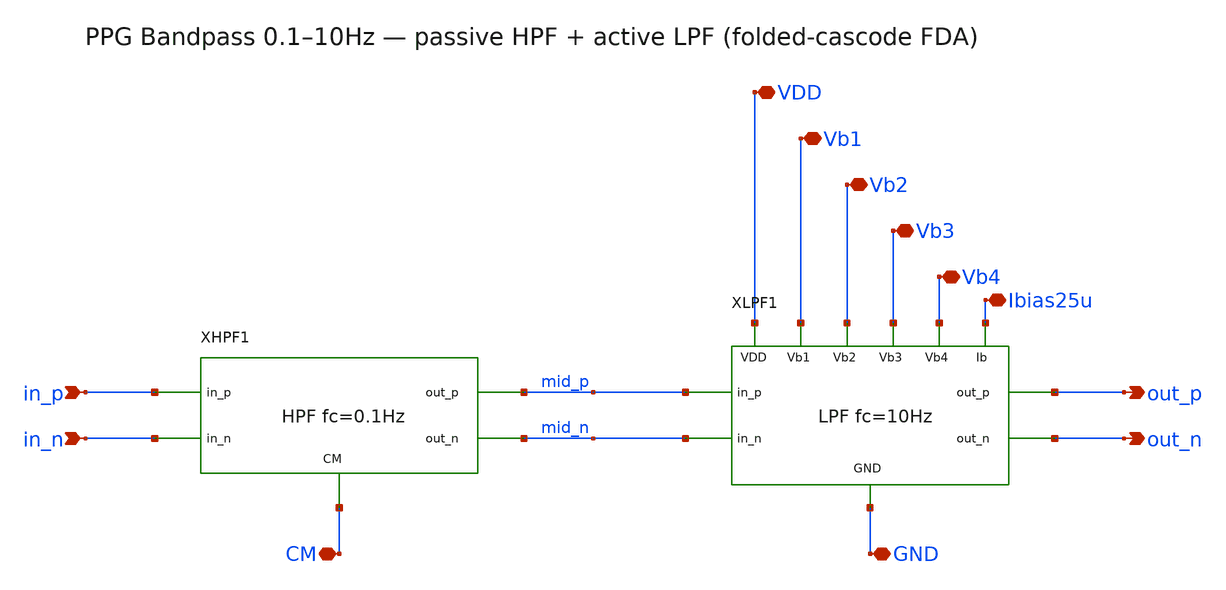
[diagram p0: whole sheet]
** sch_path: ps-filters/bandpass.sch
**.subckt bandpass in_p in_n out_p out_n CM GND VDD Vb1 Vb2 Vb3 Vb4 Ibias25u
*.ipin in_p
*.ipin in_n
*.opin out_p
*.opin out_n
*.iopin CM
*.iopin GND
*.iopin VDD
*.iopin Vb1
*.iopin Vb2
*.iopin Vb3
*.iopin Vb4
*.iopin Ibias25u
XHPF1 in_p in_n mid_p mid_n CM hpf
XLPF1 mid_p mid_n out_p out_n VDD Vb1 Vb2 Vb3 Vb4 Ibias25u GND lpf
**.ends

* expanding   symbol:  hpf.sym # of pins=5
** sym_path: ps-filters/hpf.sym
** sch_path: ps-filters/hpf.sch
.subckt hpf in_p in_n out_p out_n CM
*.ipin in_p
*.ipin in_n
*.opin out_p
*.opin out_n
*.iopin CM
Chp out_p in_p 1.59u m=1
Chn out_n in_n 1.59u m=1
Rhp out_p CM 1G m=1
Rhn out_n CM 1G m=1
.ends


* expanding   symbol:  lpf.sym # of pins=11
** sym_path: ps-filters/lpf.sym
** sch_path: ps-filters/lpf.sch
.subckt lpf in_p in_n out_p out_n VDD Vb1 Vb2 Vb3 Vb4 Ibias25u GND
*.ipin in_p
*.ipin in_n
*.opin out_p
*.opin out_n
*.iopin VDD
*.iopin GND
*.iopin Vb1
*.iopin Vb2
*.iopin Vb3
*.iopin Vb4
*.iopin Ibias25u
R1p Xp in_p 1Meg m=1
R1n Xn in_n 1Meg m=1
Rfp out_n Xp 1Meg m=1
Rfn out_p Xn 1Meg m=1
Cfp out_n Xp 15.9n m=1
Cfn out_p Xn 15.9n m=1
XFDA1 VDD Vb2 out_p out_n Vb1 Ibias25u Xn GND Xp Vb3 Vb4 foldedcasc_cmfb_forsym
.ends


* expanding   symbol:  foldedcasc_cmfb_forsym.sym # of pins=11
** sym_path: ps-filters/foldedcasc_cmfb_forsym.sym
** sch_path: ps-filters/foldedcasc_cmfb_forsym.sch
.subckt foldedcasc_cmfb_forsym VDD Vb2 Voutp Voutn Vb1 Ibias25u Vinn GND Vinp Vb3 Vb4
*.ipin VDD
*.opin Voutp
*.ipin Vinn
*.ipin Ibias25u
*.ipin GND
*.ipin Vinp
*.opin Voutn
*.ipin Vb4
*.ipin Vb1
*.ipin Vb2
*.ipin Vb3
XM5 net1 Vb3 GND GND nfet_03v3 L=0.28u W=13u nf=1 ad='int((nf+1)/2) * W/nf * 0.18u' as='int((nf+2)/2) * W/nf * 0.18u'
+ pd='2*int((nf+1)/2) * (W/nf + 0.18u)' ps='2*int((nf+2)/2) * (W/nf + 0.18u)' nrd='0.18u / W' nrs='0.18u / W'
+ sa=0 sb=0 sd=0 m=1
XM6 Voutn Vb2 net2 GND nfet_03v3 L=0.28u W=6.3u nf=1 ad='int((nf+1)/2) * W/nf * 0.18u' as='int((nf+2)/2) * W/nf * 0.18u'
+ pd='2*int((nf+1)/2) * (W/nf + 0.18u)' ps='2*int((nf+2)/2) * (W/nf + 0.18u)' nrd='0.18u / W' nrs='0.18u / W'
+ sa=0 sb=0 sd=0 m=1
XM7 Voutp Vb2 net1 GND nfet_03v3 L=0.28u W=6.3u nf=1 ad='int((nf+1)/2) * W/nf * 0.18u' as='int((nf+2)/2) * W/nf * 0.18u'
+ pd='2*int((nf+1)/2) * (W/nf + 0.18u)' ps='2*int((nf+2)/2) * (W/nf + 0.18u)' nrd='0.18u / W' nrs='0.18u / W'
+ sa=0 sb=0 sd=0 m=1
XM8 Voutn Vb1 net3 VDD pfet_03v3 L=0.28u W=19u nf=1 ad='int((nf+1)/2) * W/nf * 0.18u' as='int((nf+2)/2) * W/nf * 0.18u'
+ pd='2*int((nf+1)/2) * (W/nf + 0.18u)' ps='2*int((nf+2)/2) * (W/nf + 0.18u)' nrd='0.18u / W' nrs='0.18u / W'
+ sa=0 sb=0 sd=0 m=1
XM9 Voutp Vb1 net4 VDD pfet_03v3 L=0.28u W=19u nf=1 ad='int((nf+1)/2) * W/nf * 0.18u' as='int((nf+2)/2) * W/nf * 0.18u'
+ pd='2*int((nf+1)/2) * (W/nf + 0.18u)' ps='2*int((nf+2)/2) * (W/nf + 0.18u)' nrd='0.18u / W' nrs='0.18u / W'
+ sa=0 sb=0 sd=0 m=1
XM10 net3 Vb4 VDD VDD pfet_03v3 L=0.28u W=16.2u nf=1 ad='int((nf+1)/2) * W/nf * 0.18u' as='int((nf+2)/2) * W/nf * 0.18u'
+ pd='2*int((nf+1)/2) * (W/nf + 0.18u)' ps='2*int((nf+2)/2) * (W/nf + 0.18u)' nrd='0.18u / W' nrs='0.18u / W'
+ sa=0 sb=0 sd=0 m=1
XM11 net4 Vb4 VDD VDD pfet_03v3 L=0.28u W=16.2u nf=1 ad='int((nf+1)/2) * W/nf * 0.18u' as='int((nf+2)/2) * W/nf * 0.18u'
+ pd='2*int((nf+1)/2) * (W/nf + 0.18u)' ps='2*int((nf+2)/2) * (W/nf + 0.18u)' nrd='0.18u / W' nrs='0.18u / W'
+ sa=0 sb=0 sd=0 m=1
XM1 net1 Vinn net5 VDD pfet_03v3 L=0.28u W=3.45u nf=1 ad='int((nf+1)/2) * W/nf * 0.18u' as='int((nf+2)/2) * W/nf * 0.18u'
+ pd='2*int((nf+1)/2) * (W/nf + 0.18u)' ps='2*int((nf+2)/2) * (W/nf + 0.18u)' nrd='0.18u / W' nrs='0.18u / W'
+ sa=0 sb=0 sd=0 m=1
XM2 net2 Vinp net5 VDD pfet_03v3 L=0.28u W=3.45u nf=1 ad='int((nf+1)/2) * W/nf * 0.18u' as='int((nf+2)/2) * W/nf * 0.18u'
+ pd='2*int((nf+1)/2) * (W/nf + 0.18u)' ps='2*int((nf+2)/2) * (W/nf + 0.18u)' nrd='0.18u / W' nrs='0.18u / W'
+ sa=0 sb=0 sd=0 m=1
XM3 net5 Ibias25u net6 VDD pfet_03v3 L=0.28u W=4.9u nf=1 ad='int((nf+1)/2) * W/nf * 0.18u' as='int((nf+2)/2) * W/nf * 0.18u'
+ pd='2*int((nf+1)/2) * (W/nf + 0.18u)' ps='2*int((nf+2)/2) * (W/nf + 0.18u)' nrd='0.18u / W' nrs='0.18u / W'
+ sa=0 sb=0 sd=0 m=1
XM12 Ibias25u Ibias25u VDD VDD pfet_03v3 L=0.28u W=2.27u nf=1 ad='int((nf+1)/2) * W/nf * 0.18u' as='int((nf+2)/2) * W/nf * 0.18u'
+ pd='2*int((nf+1)/2) * (W/nf + 0.18u)' ps='2*int((nf+2)/2) * (W/nf + 0.18u)' nrd='0.18u / W' nrs='0.18u / W'
+ sa=0 sb=0 sd=0 m=1
XM13 net6 Voutp VDD VDD pfet_03v3 L=0.28u W=30u nf=1 ad='int((nf+1)/2) * W/nf * 0.18u' as='int((nf+2)/2) * W/nf * 0.18u'
+ pd='2*int((nf+1)/2) * (W/nf + 0.18u)' ps='2*int((nf+2)/2) * (W/nf + 0.18u)' nrd='0.18u / W' nrs='0.18u / W'
+ sa=0 sb=0 sd=0 m=1
XM14 net6 Voutn VDD VDD pfet_03v3 L=0.28u W=30u nf=1 ad='int((nf+1)/2) * W/nf * 0.18u' as='int((nf+2)/2) * W/nf * 0.18u'
+ pd='2*int((nf+1)/2) * (W/nf + 0.18u)' ps='2*int((nf+2)/2) * (W/nf + 0.18u)' nrd='0.18u / W' nrs='0.18u / W'
+ sa=0 sb=0 sd=0 m=1
XM4 net2 Vb3 GND GND nfet_03v3 L=0.28u W=13u nf=1 ad='int((nf+1)/2) * W/nf * 0.18u' as='int((nf+2)/2) * W/nf * 0.18u'
+ pd='2*int((nf+1)/2) * (W/nf + 0.18u)' ps='2*int((nf+2)/2) * (W/nf + 0.18u)' nrd='0.18u / W' nrs='0.18u / W'
+ sa=0 sb=0 sd=0 m=1
.ends

.end
